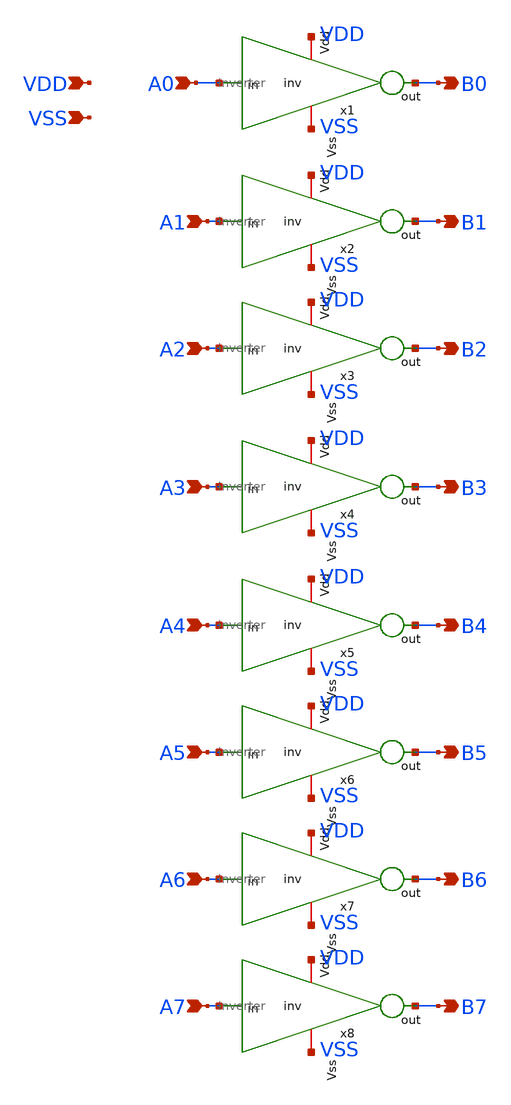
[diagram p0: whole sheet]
** sch_path: inv/inv_8bit.sch
**.subckt inv_8bit A0 A1 A2 A3 A4 A5 A6 A7 B0 B1 B2 B3 B4 B5 B6 B7 VDD VSS
*.ipin A0
*.ipin A1
*.ipin A2
*.ipin A3
*.ipin A4
*.ipin A5
*.ipin A6
*.ipin A7
*.opin B0
*.opin B1
*.opin B2
*.opin B3
*.opin B4
*.opin B5
*.opin B6
*.opin B7
*.ipin VDD
*.ipin VSS
x1 A0 VDD VSS B0 inverter
x2 A1 VDD VSS B1 inverter
x3 A2 VDD VSS B2 inverter
x4 A3 VDD VSS B3 inverter
x5 A4 VDD VSS B4 inverter
x6 A5 VDD VSS B5 inverter
x7 A6 VDD VSS B6 inverter
x8 A7 VDD VSS B7 inverter
**.ends

* expanding   symbol:  inv/inverter.sym # of pins=4
** sym_path: inv/inverter.sym
** sch_path: inv/inverter.sch
.subckt inverter in Vdd Vss out
*.ipin in
*.iopin Vdd
*.iopin Vss
*.opin out
XM2 out in Vss Vss sky130_fd_pr__nfet_01v8 L=0.15 W=1 nf=1 ad='int((1 + 1)/2) * 1 / 1 * 0.29' as='int((1 + 2)/2) * 1 / 1 * 0.29'
+ pd='2*int((1 + 1)/2) * (1 / 1 + 0.29)' ps='2*int((1 + 2)/2) * (1 / 1 + 0.29)' nrd='0.29 / 1 ' nrs='0.29 / 1 '
+ sa=0 sb=0 sd=0 mult=1 m=1
XM11 out in Vdd Vdd sky130_fd_pr__pfet_01v8 L=0.15 W=1 nf=1 ad='int((nf+1)/2) * W/nf * 0.29' as='int((nf+2)/2) * W/nf * 0.29'
+ pd='2*int((nf+1)/2) * (W/nf + 0.29)' ps='2*int((nf+2)/2) * (W/nf + 0.29)' nrd='0.29 / W' nrs='0.29 / W'
+ sa=0 sb=0 sd=0 mult=1 m=1
.ends

.end
